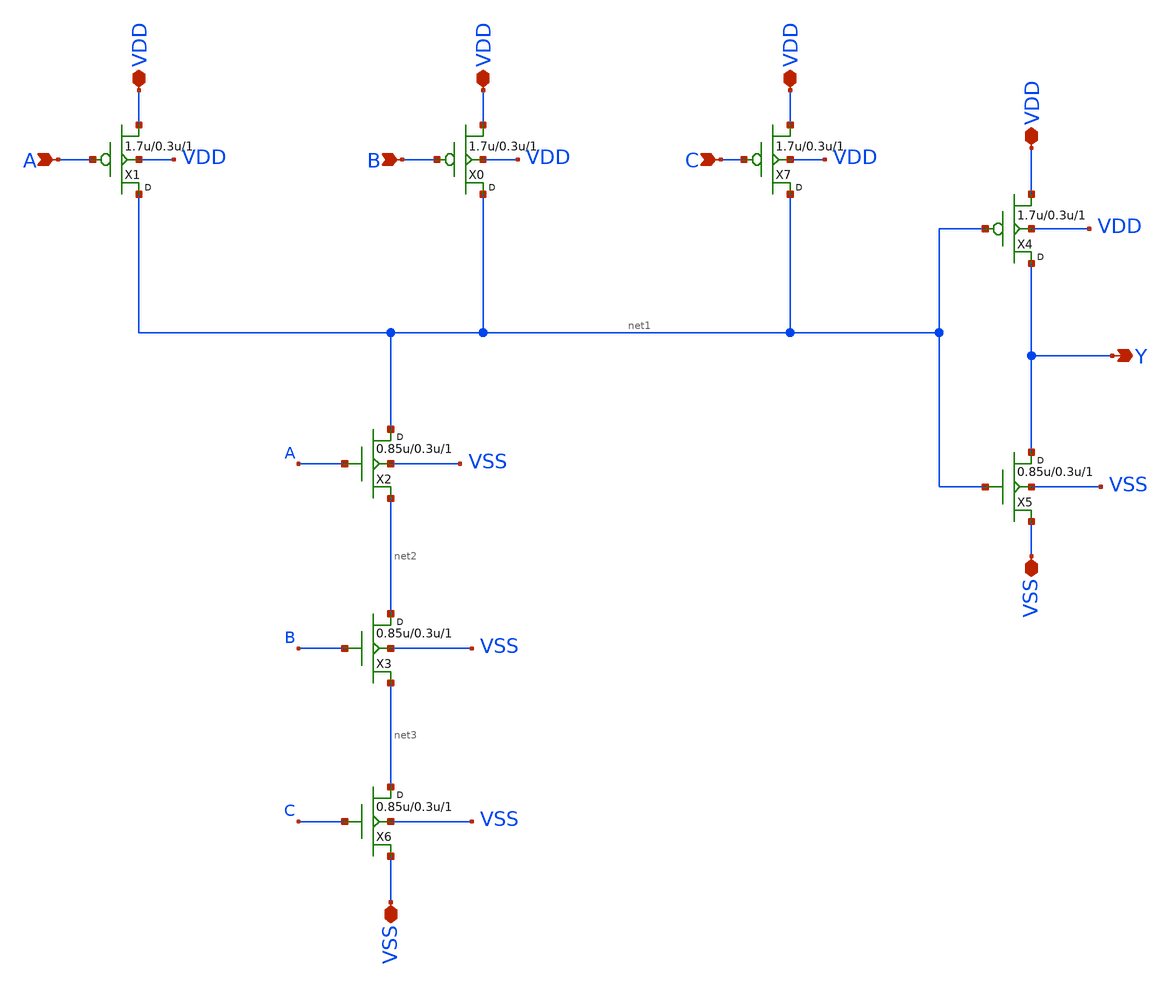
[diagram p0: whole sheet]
** sch_path: designs/libs/core_digital/gf180mcu_osu_sc_gp12t3v3/cells/and3/xschem/untitled-3.sch
**.subckt untitled-3 VDD VDD VDD VDD VSS VSS A B C Y
*.iopin VDD
*.iopin VDD
*.iopin VDD
*.iopin VDD
*.iopin VSS
*.iopin VSS
*.ipin A
*.ipin B
*.ipin C
*.opin Y
X1 net1 A VDD VDD pfet_03v3 w=1.7u l=0.3u m=1
X0 net1 B VDD VDD pfet_03v3 w=1.7u l=0.3u m=1
X7 net1 C VDD VDD pfet_03v3 w=1.7u l=0.3u m=1
X2 net1 A net2 VSS nfet_03v3 w=0.85u l=0.3u m=1
X3 net2 B net3 VSS nfet_03v3 w=0.85u l=0.3u m=1
X6 net3 C VSS VSS nfet_03v3 w=0.85u l=0.3u m=1
X4 Y net1 VDD VDD pfet_03p3 w=1.7u l=0.3u m=1
X5 Y net1 VSS VSS nfet_03p3 w=0.85u l=0.3u m=1
**.ends
.end
